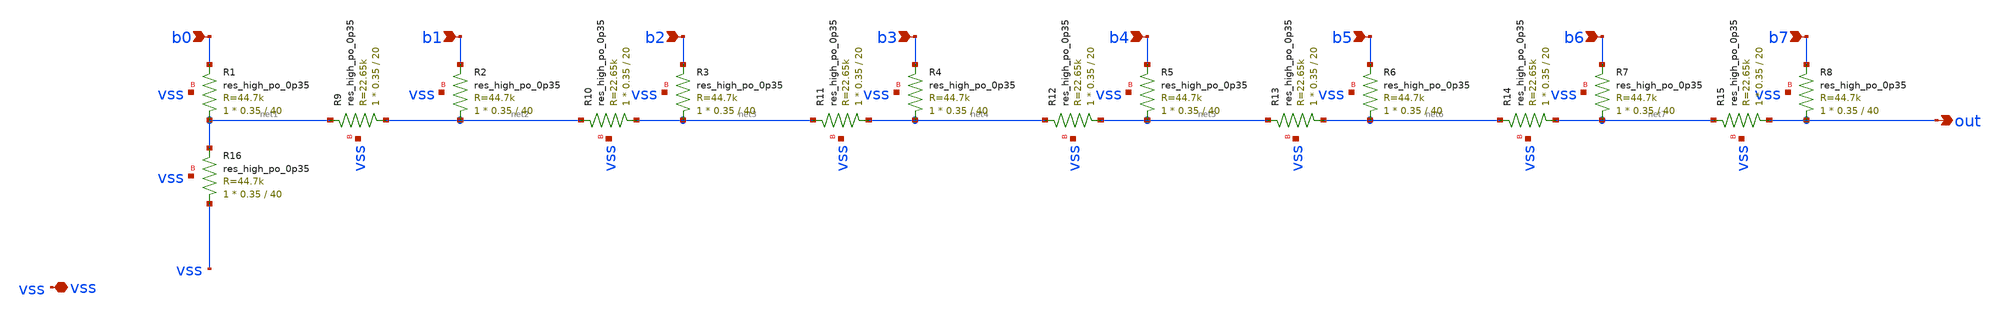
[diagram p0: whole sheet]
** sch_path: xschem/r2r.sch
**.subckt r2r b0 b1 b2 b3 b4 b5 b6 b7 out vss
*.ipin b0
*.ipin b1
*.ipin b2
*.ipin b3
*.ipin b4
*.ipin b5
*.ipin b6
*.ipin b7
*.opin out
*.iopin vss
XR1 net1 b0 vss sky130_fd_pr__res_high_po_0p35 L=40 mult=1 m=1
XR2 net2 b1 vss sky130_fd_pr__res_high_po_0p35 L=40 mult=1 m=1
XR3 net3 b2 vss sky130_fd_pr__res_high_po_0p35 L=40 mult=1 m=1
XR4 net4 b3 vss sky130_fd_pr__res_high_po_0p35 L=40 mult=1 m=1
XR5 net5 b4 vss sky130_fd_pr__res_high_po_0p35 L=40 mult=1 m=1
XR6 net6 b5 vss sky130_fd_pr__res_high_po_0p35 L=40 mult=1 m=1
XR7 net7 b6 vss sky130_fd_pr__res_high_po_0p35 L=40 mult=1 m=1
XR8 out b7 vss sky130_fd_pr__res_high_po_0p35 L=40 mult=1 m=1
XR9 net2 net1 vss sky130_fd_pr__res_high_po_0p35 L=20 mult=1 m=1
XR10 net3 net2 vss sky130_fd_pr__res_high_po_0p35 L=20 mult=1 m=1
XR11 net4 net3 vss sky130_fd_pr__res_high_po_0p35 L=20 mult=1 m=1
XR12 net5 net4 vss sky130_fd_pr__res_high_po_0p35 L=20 mult=1 m=1
XR13 net6 net5 vss sky130_fd_pr__res_high_po_0p35 L=20 mult=1 m=1
XR14 net7 net6 vss sky130_fd_pr__res_high_po_0p35 L=20 mult=1 m=1
XR15 out net7 vss sky130_fd_pr__res_high_po_0p35 L=20 mult=1 m=1
XR16 vss net1 vss sky130_fd_pr__res_high_po_0p35 L=40 mult=1 m=1
**.ends
.end
